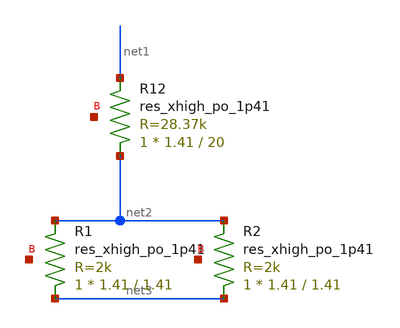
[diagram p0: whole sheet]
** sch_path: sch/ex1.sch
**.subckt ex1
XR12 net2 net1 net4 sky130_fd_pr__res_xhigh_po_1p41 L=20 mult=1 m=1
XR1 net3 net2 net5 sky130_fd_pr__res_xhigh_po_1p41 L=1.41 mult=1 m=1
XR2 net3 net2 net6 sky130_fd_pr__res_xhigh_po_1p41 L=1.41 mult=1 m=1
**.ends
.end
